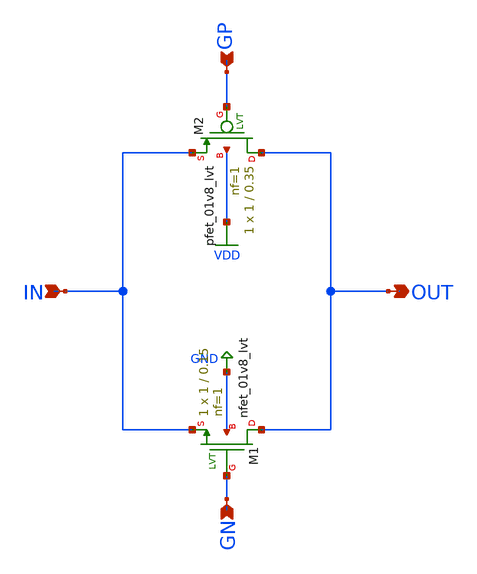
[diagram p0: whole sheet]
** sch_path: xschem/transmission_gate.sch
**.subckt transmission_gate OUT IN GN GP
*.opin OUT
*.ipin IN
*.ipin GN
*.ipin GP
XM1 OUT GN IN GND sky130_fd_pr__nfet_01v8_lvt L=0.15 W=1 nf=1 ad='int((nf+1)/2) * W/nf * 0.29' as='int((nf+2)/2) * W/nf * 0.29'
+ pd='2*int((nf+1)/2) * (W/nf + 0.29)' ps='2*int((nf+2)/2) * (W/nf + 0.29)' nrd='0.29 / W' nrs='0.29 / W'
+ sa=0 sb=0 sd=0 mult=1 m=1
XM2 OUT GP IN VDD sky130_fd_pr__pfet_01v8_lvt L=0.35 W=1 nf=1 ad='int((nf+1)/2) * W/nf * 0.29' as='int((nf+2)/2) * W/nf * 0.29'
+ pd='2*int((nf+1)/2) * (W/nf + 0.29)' ps='2*int((nf+2)/2) * (W/nf + 0.29)' nrd='0.29 / W' nrs='0.29 / W'
+ sa=0 sb=0 sd=0 mult=1 m=1
**.ends
.GLOBAL GND
.GLOBAL VDD
.end
